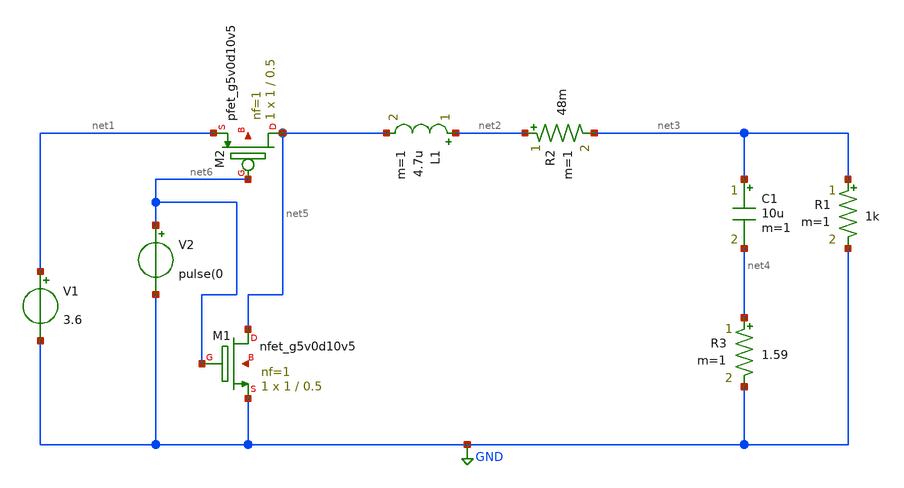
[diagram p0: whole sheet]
** sch_path: Abishek_Sam_group/Buck_converter.sch
**.subckt Buck_converter
XM1 net5 net6 GND net7 sky130_fd_pr__nfet_g5v0d10v5 L=0.5 W=1 nf=1 ad='int((nf+1)/2) * W/nf * 0.29' as='int((nf+2)/2) * W/nf * 0.29'
+ pd='2*int((nf+1)/2) * (W/nf + 0.29)' ps='2*int((nf+2)/2) * (W/nf + 0.29)' nrd='0.29 / W' nrs='0.29 / W'
+ sa=0 sb=0 sd=0 mult=1 m=1
XM2 net5 net6 net1 net8 sky130_fd_pr__pfet_g5v0d10v5 L=0.5 W=1 nf=1 ad='int((nf+1)/2) * W/nf * 0.29'
+ as='int((nf+2)/2) * W/nf * 0.29' pd='2*int((nf+1)/2) * (W/nf + 0.29)' ps='2*int((nf+2)/2) * (W/nf + 0.29)'
+ nrd='0.29 / W' nrs='0.29 / W' sa=0 sb=0 sd=0 mult=1 m=1
C1 net3 net4 10u m=1
L1 net2 net5 4.7u m=1
R1 net3 GND 1k m=1
V1 net1 GND 3.6
R2 net2 net3 48m m=1
R3 net4 GND 1.59 m=1
V2 net6 GND pulse(0
**.ends
.GLOBAL GND
.end
